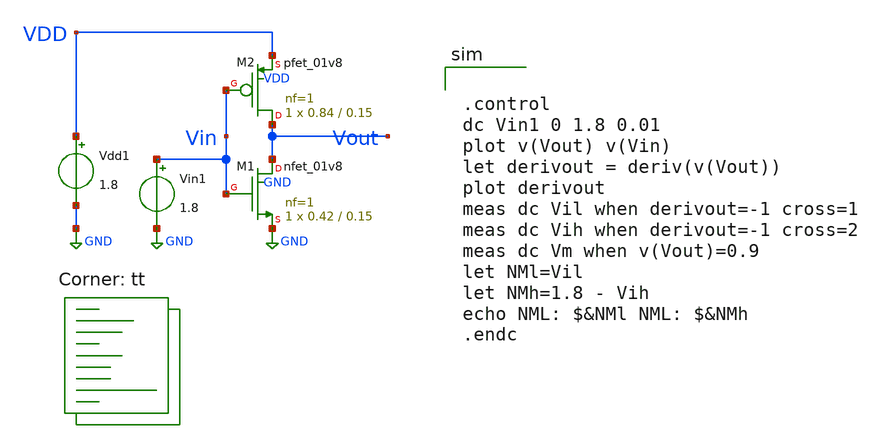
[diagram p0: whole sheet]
** sch_path: tutorial_3/tutorial_3_1a.sch
**.subckt tutorial_3_1a
XM1 Vout Vin GND GND sky130_fd_pr__nfet_01v8 L=0.15 W=0.42 nf=1 ad='int((nf+1)/2) * W/nf * 0.29' as='int((nf+2)/2) * W/nf * 0.29'
+ pd='2*int((nf+1)/2) * (W/nf + 0.29)' ps='2*int((nf+2)/2) * (W/nf + 0.29)' nrd='0.29 / W' nrs='0.29 / W'
+ sa=0 sb=0 sd=0 mult=1 m=1
XM2 Vout Vin VDD VDD sky130_fd_pr__pfet_01v8 L=0.15 W=0.84 nf=1 ad='int((nf+1)/2) * W/nf * 0.29' as='int((nf+2)/2) * W/nf * 0.29'
+ pd='2*int((nf+1)/2) * (W/nf + 0.29)' ps='2*int((nf+2)/2) * (W/nf + 0.29)' nrd='0.29 / W' nrs='0.29 / W'
+ sa=0 sb=0 sd=0 mult=1 m=1
Vin1 Vin GND 1.8
Vdd1 VDD GND 1.8
**** begin user architecture code


.control
dc Vin1 0 1.8 0.01
plot v(Vout) v(Vin)
let derivout = deriv(v(Vout))
plot derivout
meas dc Vil when derivout=-1 cross=1
meas dc Vih when derivout=-1 cross=2
meas dc Vm when v(Vout)=0.9
let NMl=Vil
let NMh=1.8 - Vih
echo NML: $&NMl NML: $&NMh
.endc

.lib $::SKYWATER_MODELS/sky130.lib.spice tt
**** end user architecture code
**.ends
.GLOBAL GND
.end
